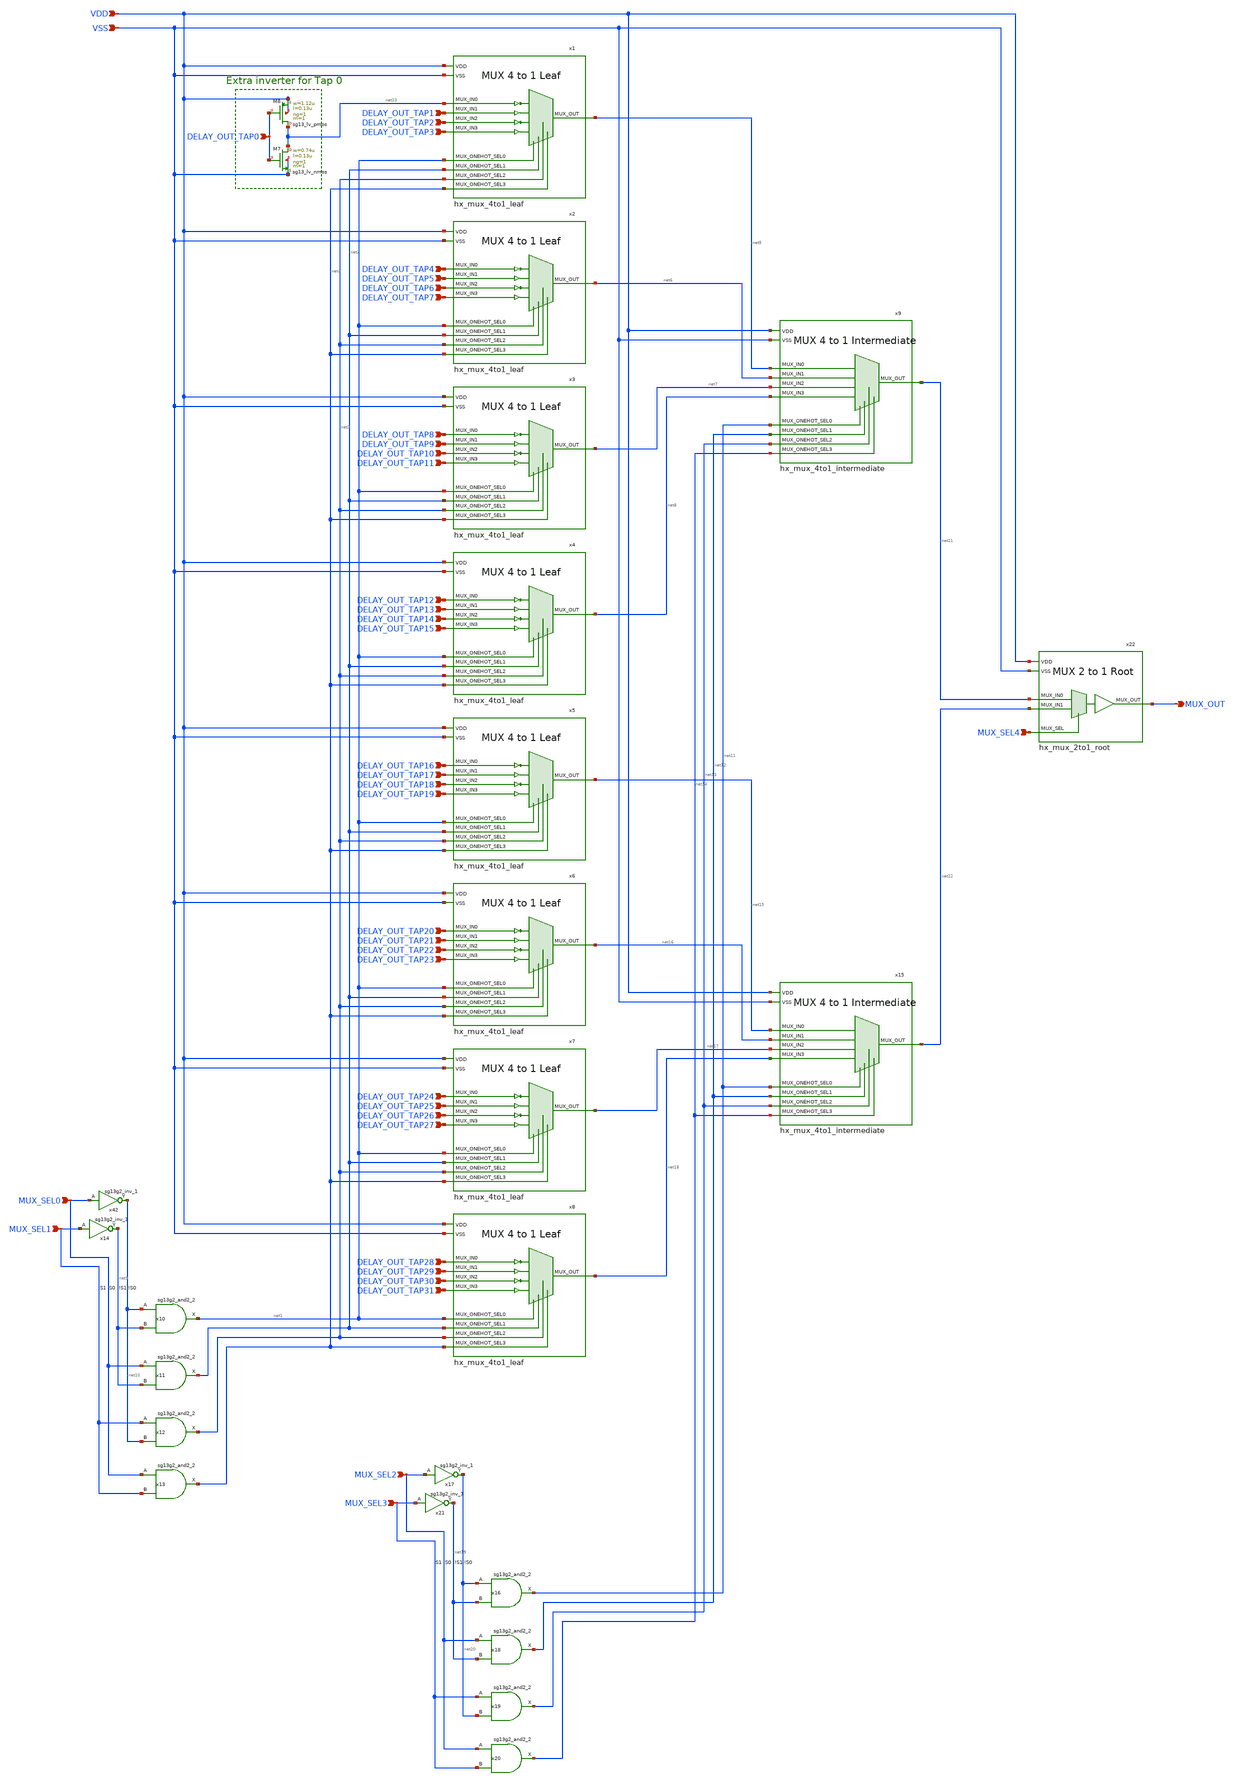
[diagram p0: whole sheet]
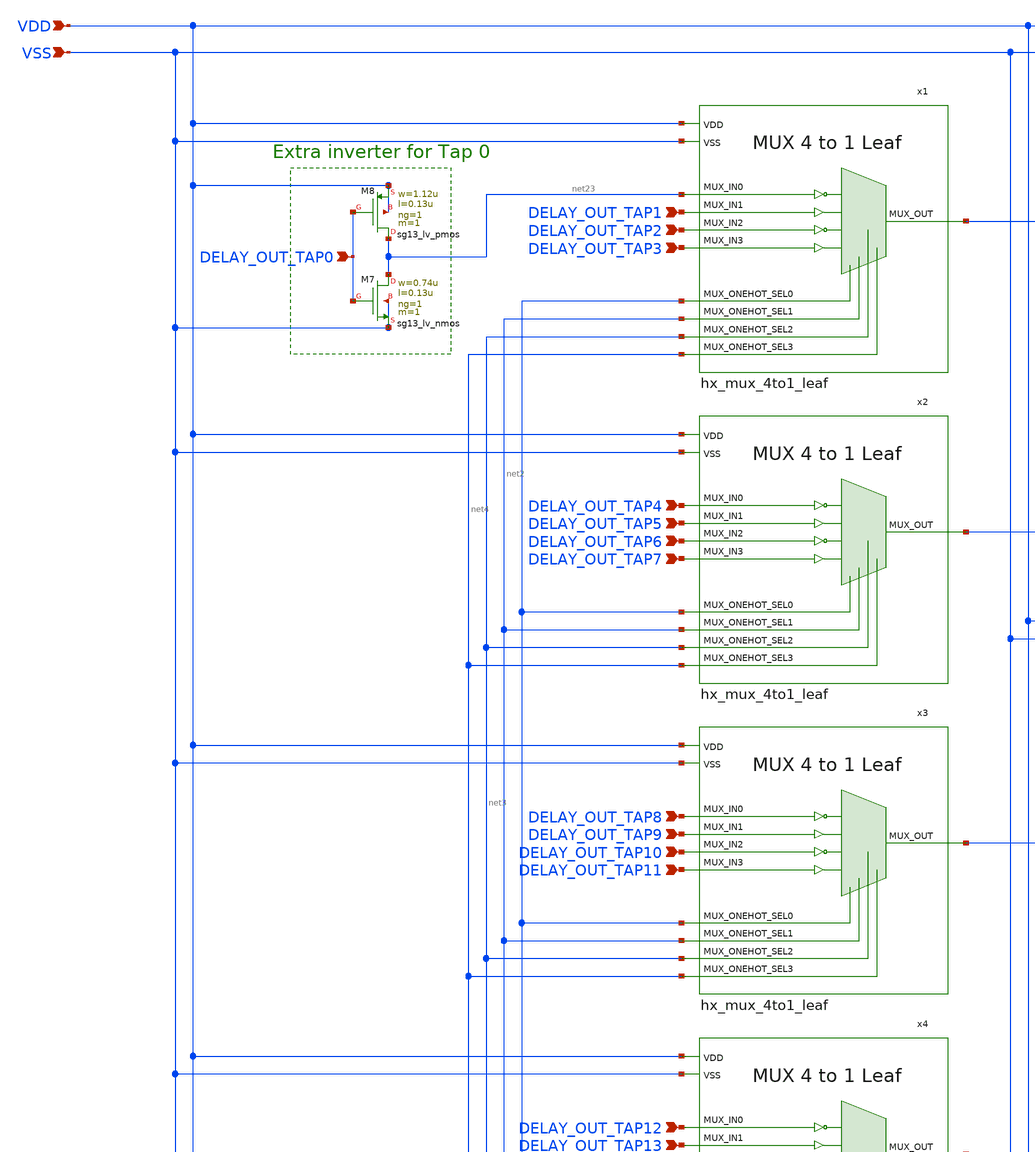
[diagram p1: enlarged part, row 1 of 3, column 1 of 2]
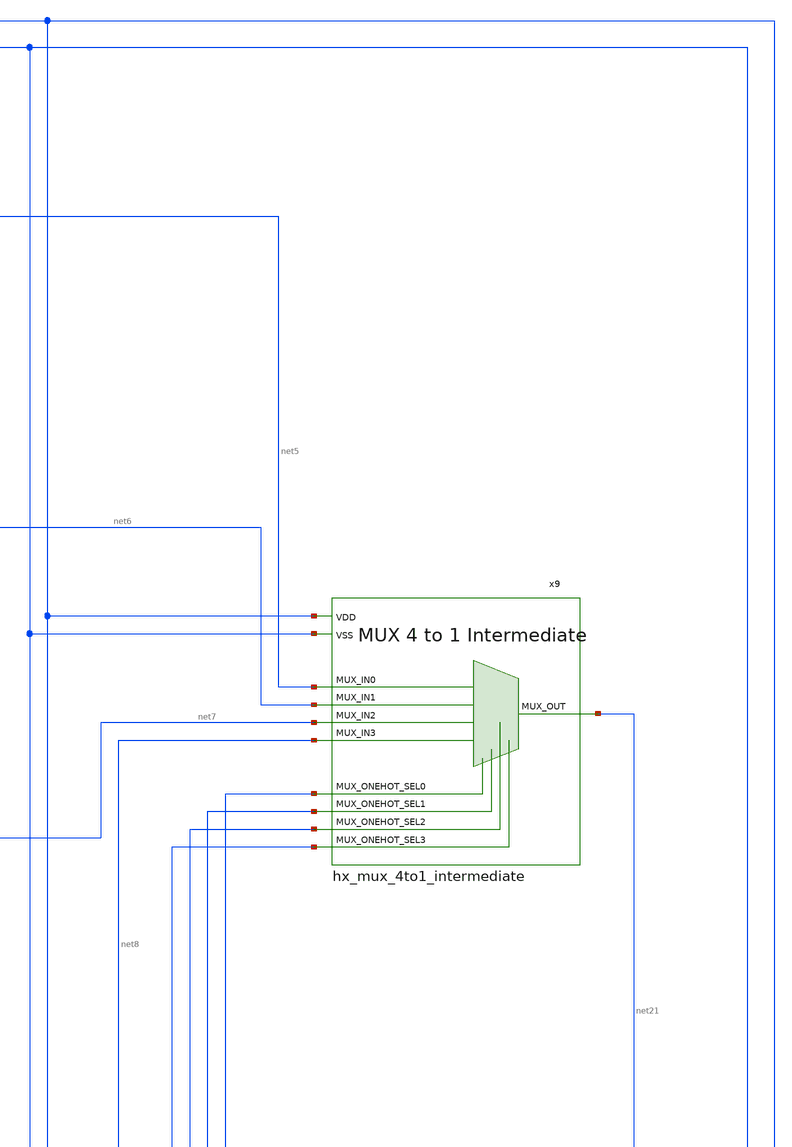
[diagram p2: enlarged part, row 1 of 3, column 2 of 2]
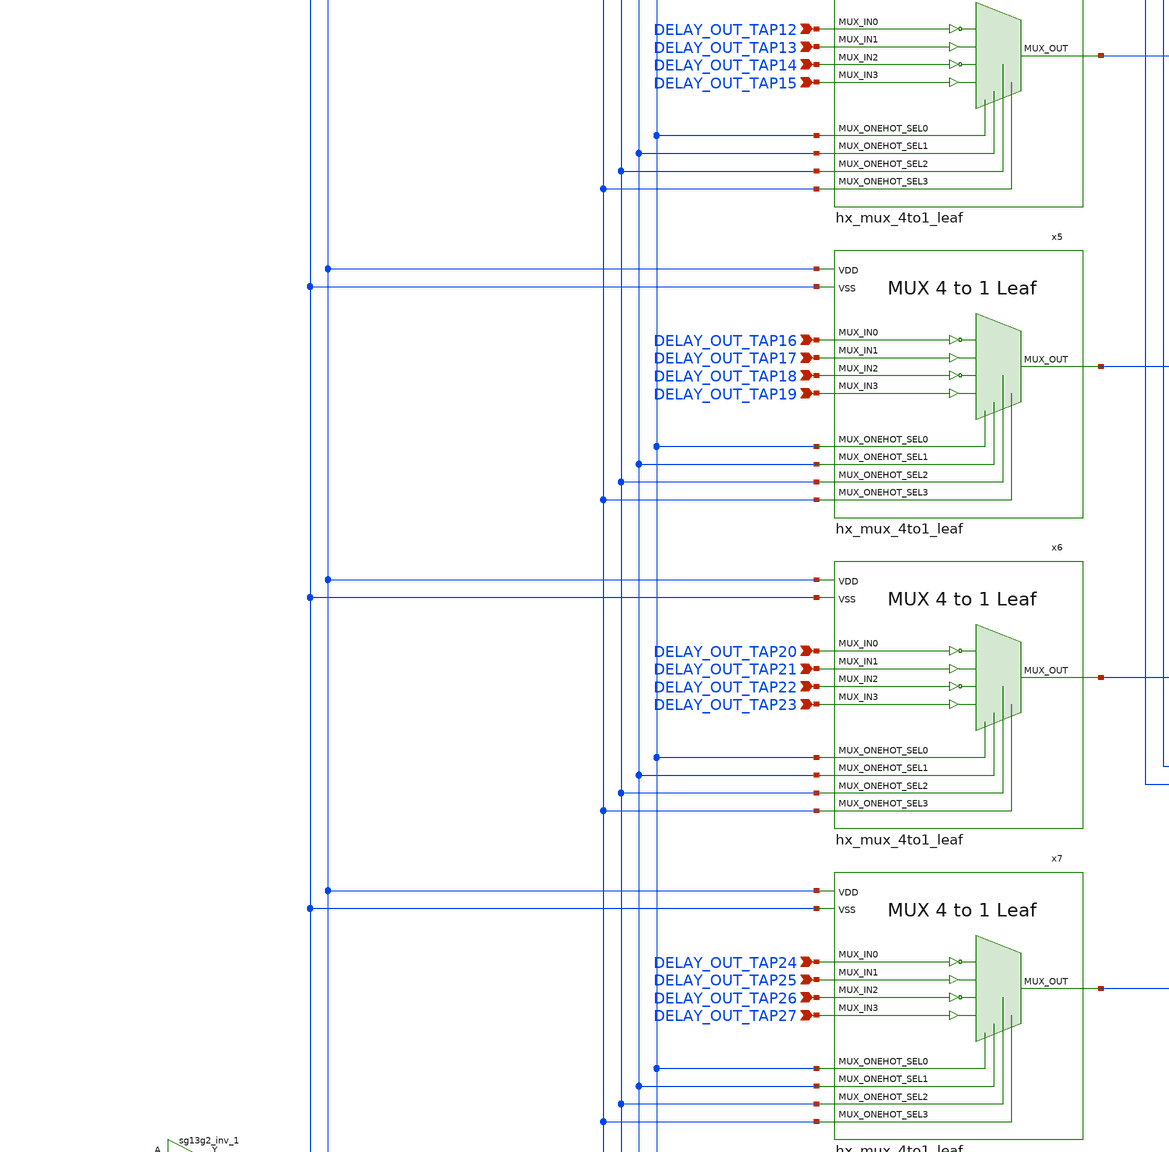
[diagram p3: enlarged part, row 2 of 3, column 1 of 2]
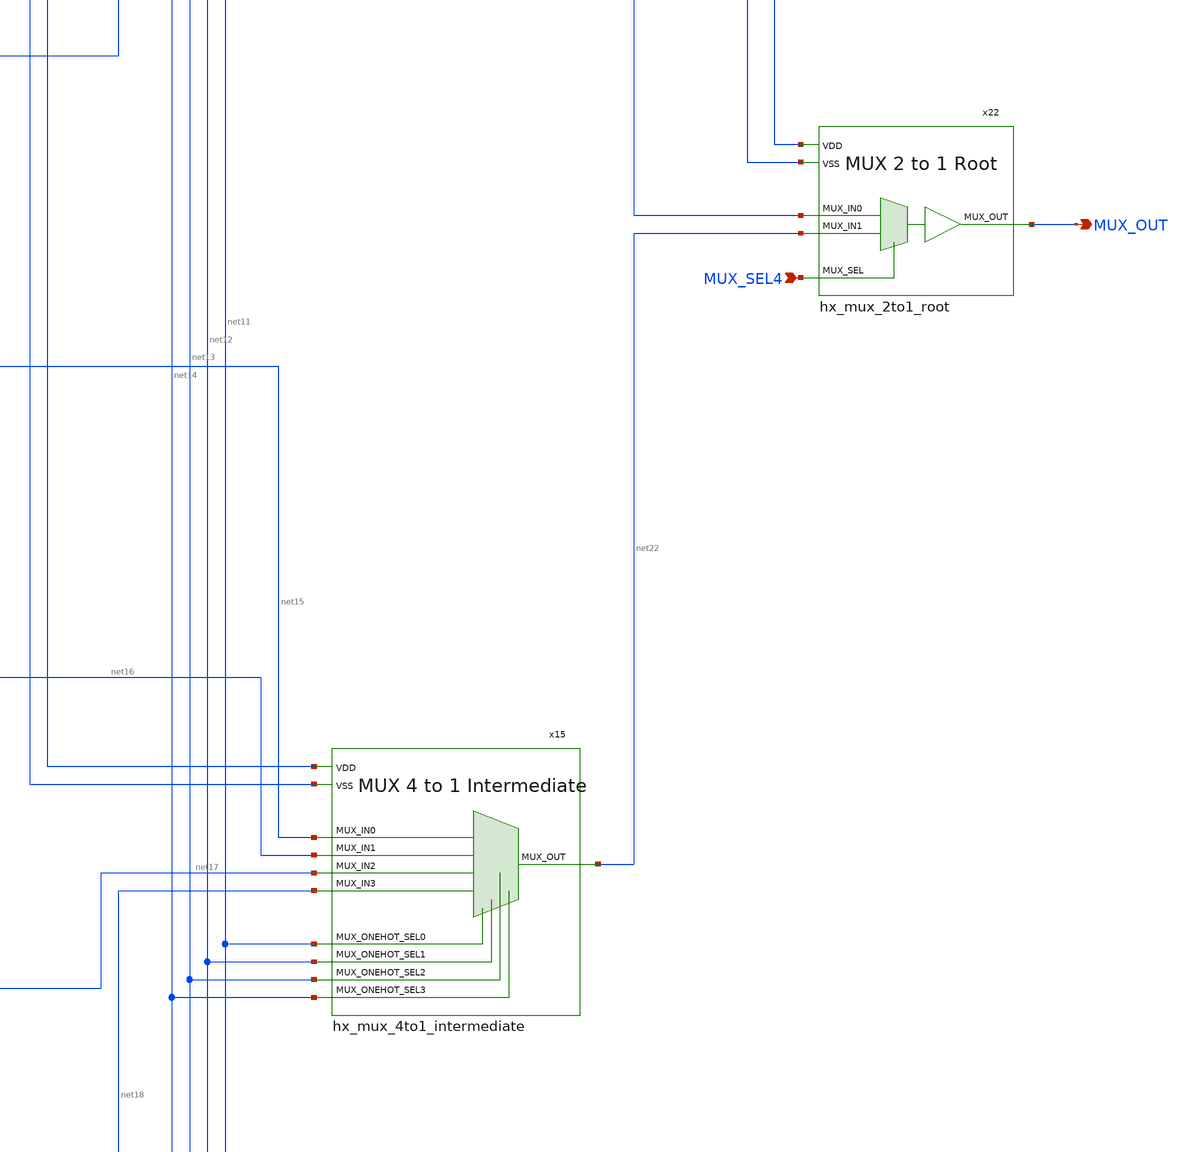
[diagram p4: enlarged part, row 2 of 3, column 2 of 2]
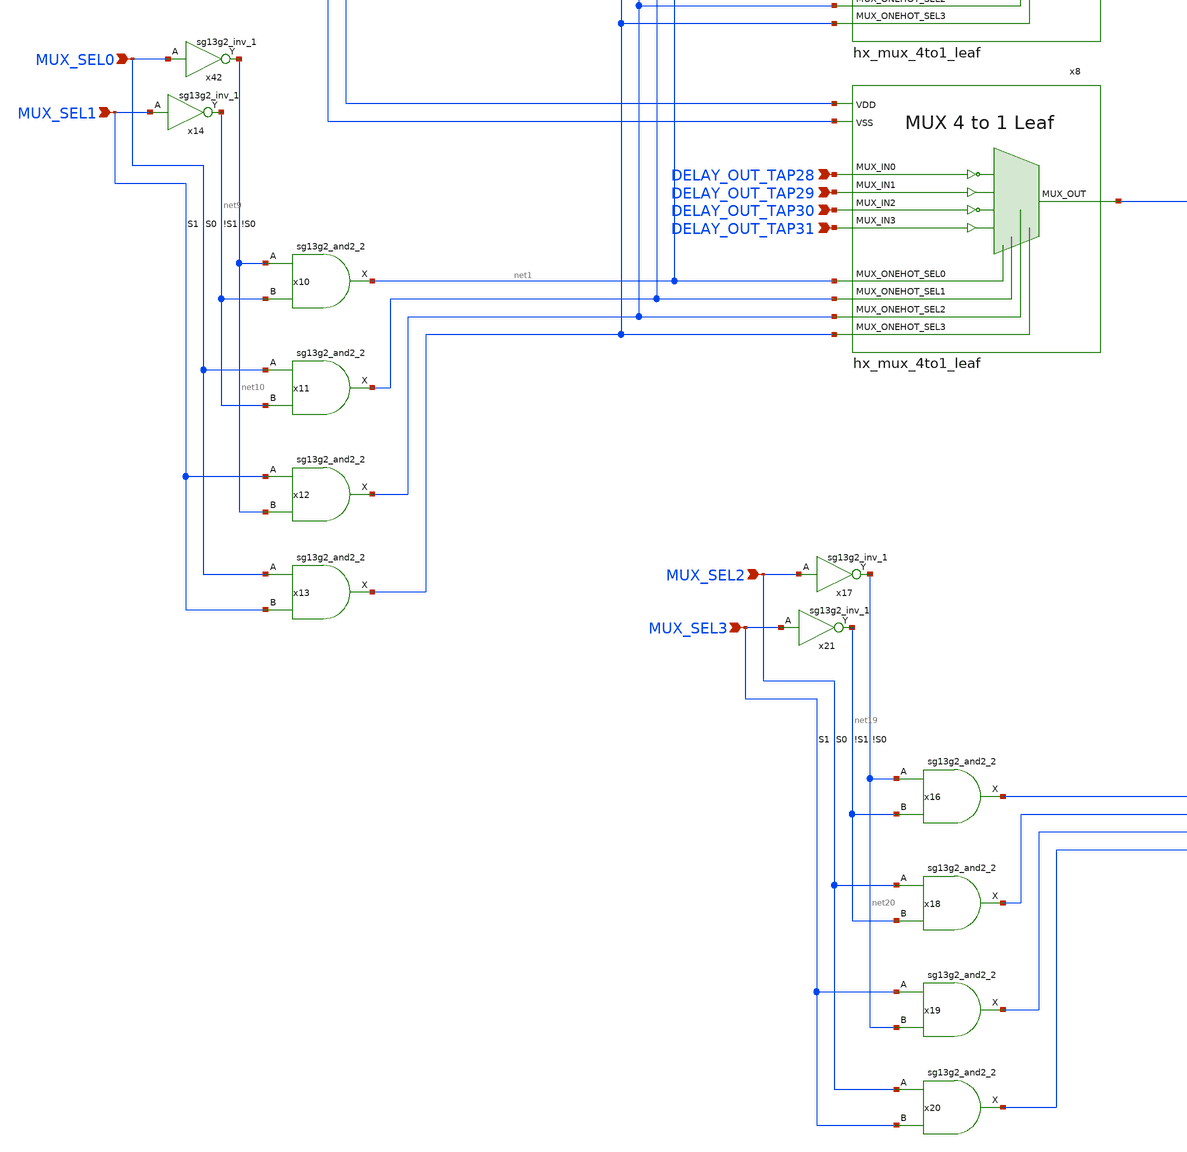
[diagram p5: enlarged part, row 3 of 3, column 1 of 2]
** sch_path: schematics/hx_mux.sch
**.subckt hx_mux VDD VSS DELAY_OUT_TAP0 MUX_OUT DELAY_OUT_TAP1 DELAY_OUT_TAP2 DELAY_OUT_TAP3
*+ MUX_SEL0 MUX_SEL1 MUX_SEL4 DELAY_OUT_TAP4 DELAY_OUT_TAP5 DELAY_OUT_TAP6 DELAY_OUT_TAP7 DELAY_OUT_TAP8
*+ DELAY_OUT_TAP9 DELAY_OUT_TAP11 DELAY_OUT_TAP10 DELAY_OUT_TAP12 DELAY_OUT_TAP13 DELAY_OUT_TAP15 DELAY_OUT_TAP14
*+ DELAY_OUT_TAP16 DELAY_OUT_TAP17 DELAY_OUT_TAP19 DELAY_OUT_TAP18 DELAY_OUT_TAP20 DELAY_OUT_TAP21 DELAY_OUT_TAP23
*+ DELAY_OUT_TAP22 DELAY_OUT_TAP24 DELAY_OUT_TAP25 DELAY_OUT_TAP27 DELAY_OUT_TAP26 DELAY_OUT_TAP28 DELAY_OUT_TAP29
*+ DELAY_OUT_TAP31 DELAY_OUT_TAP30 MUX_SEL2 MUX_SEL3
*.ipin VDD
*.ipin VSS
*.ipin DELAY_OUT_TAP0
*.opin MUX_OUT
*.ipin DELAY_OUT_TAP1
*.ipin DELAY_OUT_TAP2
*.ipin DELAY_OUT_TAP3
*.ipin MUX_SEL0
*.ipin MUX_SEL1
*.ipin MUX_SEL4
*.ipin DELAY_OUT_TAP4
*.ipin DELAY_OUT_TAP5
*.ipin DELAY_OUT_TAP6
*.ipin DELAY_OUT_TAP7
*.ipin DELAY_OUT_TAP8
*.ipin DELAY_OUT_TAP9
*.ipin DELAY_OUT_TAP11
*.ipin DELAY_OUT_TAP10
*.ipin DELAY_OUT_TAP12
*.ipin DELAY_OUT_TAP13
*.ipin DELAY_OUT_TAP15
*.ipin DELAY_OUT_TAP14
*.ipin DELAY_OUT_TAP16
*.ipin DELAY_OUT_TAP17
*.ipin DELAY_OUT_TAP19
*.ipin DELAY_OUT_TAP18
*.ipin DELAY_OUT_TAP20
*.ipin DELAY_OUT_TAP21
*.ipin DELAY_OUT_TAP23
*.ipin DELAY_OUT_TAP22
*.ipin DELAY_OUT_TAP24
*.ipin DELAY_OUT_TAP25
*.ipin DELAY_OUT_TAP27
*.ipin DELAY_OUT_TAP26
*.ipin DELAY_OUT_TAP28
*.ipin DELAY_OUT_TAP29
*.ipin DELAY_OUT_TAP31
*.ipin DELAY_OUT_TAP30
*.ipin MUX_SEL2
*.ipin MUX_SEL3
x1 VSS net3 net4 net1 net2 DELAY_OUT_TAP1 DELAY_OUT_TAP2 DELAY_OUT_TAP3 net23 VDD net5
+ hx_mux_4to1_leaf
x2 VSS net3 net4 net1 net2 DELAY_OUT_TAP5 DELAY_OUT_TAP6 DELAY_OUT_TAP7 DELAY_OUT_TAP4 VDD net6
+ hx_mux_4to1_leaf
x3 VSS net3 net4 net1 net2 DELAY_OUT_TAP9 DELAY_OUT_TAP10 DELAY_OUT_TAP11 DELAY_OUT_TAP8 VDD net7
+ hx_mux_4to1_leaf
x4 VSS net3 net4 net1 net2 DELAY_OUT_TAP13 DELAY_OUT_TAP14 DELAY_OUT_TAP15 DELAY_OUT_TAP12 VDD net8
+ hx_mux_4to1_leaf
x5 VSS net3 net4 net1 net2 DELAY_OUT_TAP17 DELAY_OUT_TAP18 DELAY_OUT_TAP19 DELAY_OUT_TAP16 VDD net15
+ hx_mux_4to1_leaf
x6 VSS net3 net4 net1 net2 DELAY_OUT_TAP21 DELAY_OUT_TAP22 DELAY_OUT_TAP23 DELAY_OUT_TAP20 VDD net16
+ hx_mux_4to1_leaf
x7 VSS net3 net4 net1 net2 DELAY_OUT_TAP25 DELAY_OUT_TAP26 DELAY_OUT_TAP27 DELAY_OUT_TAP24 VDD net17
+ hx_mux_4to1_leaf
x8 VSS net3 net4 net1 net2 DELAY_OUT_TAP29 DELAY_OUT_TAP30 DELAY_OUT_TAP31 DELAY_OUT_TAP28 VDD net18
+ hx_mux_4to1_leaf
x9 VSS VDD net11 net12 net13 net14 net21 net5 net6 net7 net8 hx_mux_4to1_intermediate
x10 net1 net10 net9 VDD VSS sg13g2_and2_2
x42 net10 MUX_SEL0 VDD VSS sg13g2_inv_1
x11 net2 MUX_SEL0 net9 VDD VSS sg13g2_and2_2
x12 net3 MUX_SEL1 net10 VDD VSS sg13g2_and2_2
x13 net4 MUX_SEL0 MUX_SEL1 VDD VSS sg13g2_and2_2
x14 net9 MUX_SEL1 VDD VSS sg13g2_inv_1
x15 VSS VDD net11 net12 net13 net14 net22 net15 net16 net17 net18 hx_mux_4to1_intermediate
x16 net11 net20 net19 VDD VSS sg13g2_and2_2
x17 net20 MUX_SEL2 VDD VSS sg13g2_inv_1
x18 net12 MUX_SEL2 net19 VDD VSS sg13g2_and2_2
x19 net13 MUX_SEL3 net20 VDD VSS sg13g2_and2_2
x20 net14 MUX_SEL2 MUX_SEL3 VDD VSS sg13g2_and2_2
x21 net19 MUX_SEL3 VDD VSS sg13g2_inv_1
x22 VSS VDD MUX_OUT MUX_SEL4 net22 net21 hx_mux_2to1_root
XM7 net23 DELAY_OUT_TAP0 VSS VSS sg13_lv_nmos w=0.74u l=0.13u ng=1 m=1 mm_ok=1
XM8 net23 DELAY_OUT_TAP0 VDD VDD sg13_lv_pmos w=1.12u l=0.13u ng=1 m=1 mm_ok=1
**.ends

* expanding   symbol:  sg13g2_and2_2.sym # of pins=3
** sym_path: sg13g2_and2_2.sym
** sch_path: sg13g2_and2_2.sch
.subckt sg13g2_and2_2 X A B VDD VSS
*.ipin A
*.ipin B
*.opin X
*.iopin VDD
*.iopin VSS
XM1 net1 A net2 VSS sg13_lv_nmos w=640.00n l=130.00n ng=1 m=1 mm_ok=1
XM2 net2 B VSS VSS sg13_lv_nmos w=640.00n l=130.00n ng=1 m=1 mm_ok=1
XM3 X net1 VSS VSS sg13_lv_nmos w=1.48u l=130.00n ng=2 m=1 mm_ok=1
XM4 net1 B VDD VDD sg13_lv_pmos w=840.00n l=130.00n ng=1 m=1 mm_ok=1
XM5 net1 A VDD VDD sg13_lv_pmos w=840.00n l=130.00n ng=1 m=1 mm_ok=1
XM6 X net1 VDD VDD sg13_lv_pmos w=2.24u l=130.00n ng=2 m=1 mm_ok=1
.ends


* expanding   symbol:  sg13g2_inv_1.sym # of pins=2
** sym_path: sg13g2_inv_1.sym
** sch_path: sg13g2_inv_1.sch
.subckt sg13g2_inv_1 Y A VDD VSS
*.opin Y
*.ipin A
*.iopin VDD
*.iopin VSS
XM1 Y A VSS VSS sg13_lv_nmos w=740.00n l=130.00n ng=1 m=1 mm_ok=1
XM2 Y A VDD VDD sg13_lv_pmos w=1.12u l=130.00n ng=1 m=1 mm_ok=1
.ends

.end
